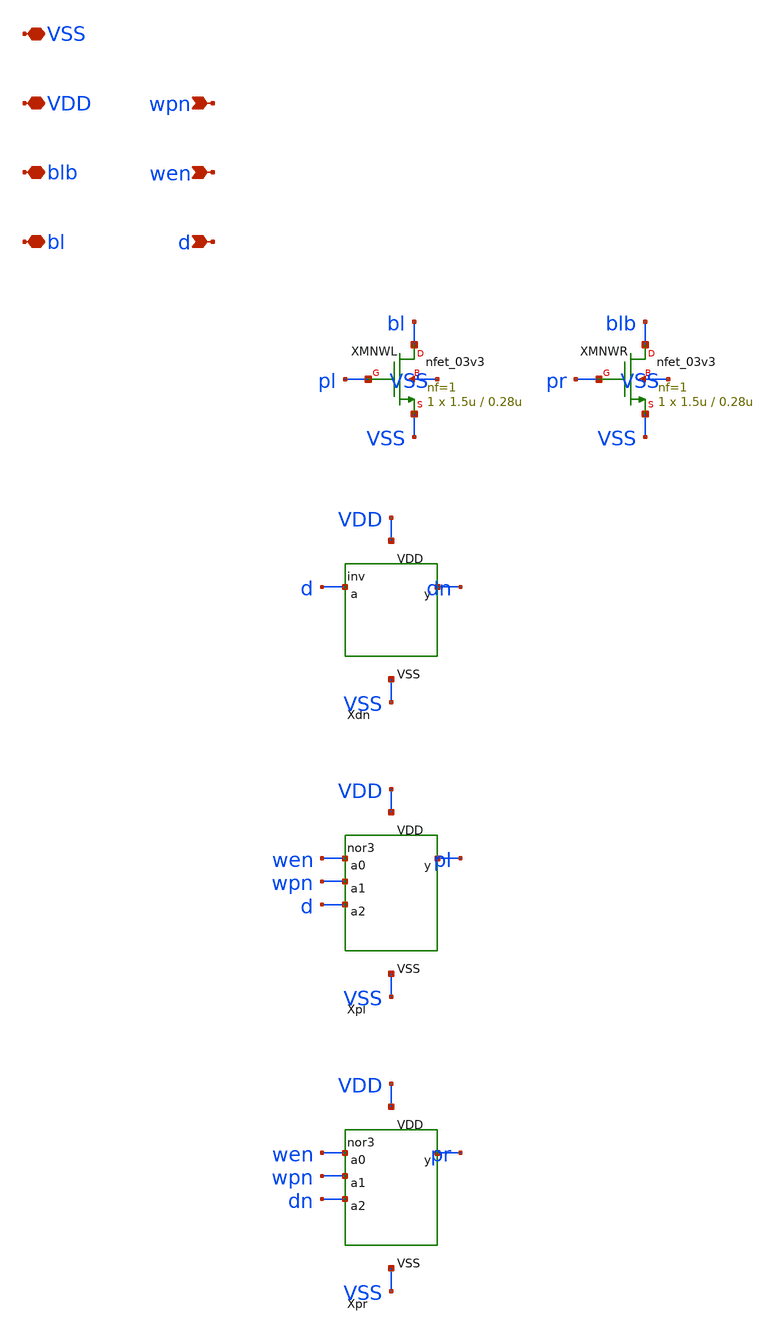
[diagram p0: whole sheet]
** sch_path: design/wdrv.sch
**.subckt wdrv d wen wpn bl blb VDD VSS
*.ipin d
*.ipin wen
*.ipin wpn
*.iopin bl
*.iopin blb
*.iopin VDD
*.iopin VSS
XMNWL bl pl VSS VSS nfet_03v3 L=0.28u W=1.5u nf=1 ad='int((nf+1)/2) * W/nf * 0.18u' as='int((nf+2)/2) * W/nf * 0.18u'
+ pd='2*int((nf+1)/2) * (W/nf + 0.18u)' ps='2*int((nf+2)/2) * (W/nf + 0.18u)' nrd='0.18u / W' nrs='0.18u / W'
+ sa=0 sb=0 sd=0 m=1
XMNWR blb pr VSS VSS nfet_03v3 L=0.28u W=1.5u nf=1 ad='int((nf+1)/2) * W/nf * 0.18u' as='int((nf+2)/2) * W/nf * 0.18u'
+ pd='2*int((nf+1)/2) * (W/nf + 0.18u)' ps='2*int((nf+2)/2) * (W/nf + 0.18u)' nrd='0.18u / W' nrs='0.18u / W'
+ sa=0 sb=0 sd=0 m=1
XXdn d dn VDD VSS inv
XXpl wen wpn d pl VDD VSS nor3
XXpr wen wpn dn pr VDD VSS nor3
**.ends

* expanding   symbol:  inv.sym # of pins=4
** sym_path: design/inv.sym
** sch_path: design/inv.sch
.subckt inv a y VDD VSS

*.ipin a
*.opin y
*.iopin VDD
*.iopin VSS
XMP y a VDD VDD pfet_03v3 L=0.28u W=1u nf=1 ad='int((nf+1)/2) * W/nf * 0.18u' as='int((nf+2)/2) * W/nf * 0.18u'
+ pd='2*int((nf+1)/2) * (W/nf + 0.18u)' ps='2*int((nf+2)/2) * (W/nf + 0.18u)' nrd='0.18u / W' nrs='0.18u / W'
+ sa=0 sb=0 sd=0 m=1
XMN y a VSS VSS nfet_03v3 L=0.28u W=0.5u nf=1 ad='int((nf+1)/2) * W/nf * 0.18u' as='int((nf+2)/2) * W/nf * 0.18u'
+ pd='2*int((nf+1)/2) * (W/nf + 0.18u)' ps='2*int((nf+2)/2) * (W/nf + 0.18u)' nrd='0.18u / W' nrs='0.18u / W'
+ sa=0 sb=0 sd=0 m=1
.ends


* expanding   symbol:  nor3.sym # of pins=6
** sym_path: design/nor3.sym
** sch_path: design/nor3.sch
.subckt nor3 a0 a1 a2 y VDD VSS

*.ipin a0
*.ipin a1
*.ipin a2
*.opin y
*.iopin VDD
*.iopin VSS
XMP0 t1 a0 VDD VDD pfet_03v3 L=0.28u W=2u nf=1 ad='int((nf+1)/2) * W/nf * 0.18u' as='int((nf+2)/2) * W/nf * 0.18u'
+ pd='2*int((nf+1)/2) * (W/nf + 0.18u)' ps='2*int((nf+2)/2) * (W/nf + 0.18u)' nrd='0.18u / W' nrs='0.18u / W'
+ sa=0 sb=0 sd=0 m=1
XMP1 t2 a1 t1 VDD pfet_03v3 L=0.28u W=2u nf=1 ad='int((nf+1)/2) * W/nf * 0.18u' as='int((nf+2)/2) * W/nf * 0.18u'
+ pd='2*int((nf+1)/2) * (W/nf + 0.18u)' ps='2*int((nf+2)/2) * (W/nf + 0.18u)' nrd='0.18u / W' nrs='0.18u / W'
+ sa=0 sb=0 sd=0 m=1
XMP2 y a2 t2 VDD pfet_03v3 L=0.28u W=2u nf=1 ad='int((nf+1)/2) * W/nf * 0.18u' as='int((nf+2)/2) * W/nf * 0.18u'
+ pd='2*int((nf+1)/2) * (W/nf + 0.18u)' ps='2*int((nf+2)/2) * (W/nf + 0.18u)' nrd='0.18u / W' nrs='0.18u / W'
+ sa=0 sb=0 sd=0 m=1
XMN0 y a0 VSS VSS nfet_03v3 L=0.28u W=0.5u nf=1 ad='int((nf+1)/2) * W/nf * 0.18u' as='int((nf+2)/2) * W/nf * 0.18u'
+ pd='2*int((nf+1)/2) * (W/nf + 0.18u)' ps='2*int((nf+2)/2) * (W/nf + 0.18u)' nrd='0.18u / W' nrs='0.18u / W'
+ sa=0 sb=0 sd=0 m=1
XMN1 y a1 VSS VSS nfet_03v3 L=0.28u W=0.5u nf=1 ad='int((nf+1)/2) * W/nf * 0.18u' as='int((nf+2)/2) * W/nf * 0.18u'
+ pd='2*int((nf+1)/2) * (W/nf + 0.18u)' ps='2*int((nf+2)/2) * (W/nf + 0.18u)' nrd='0.18u / W' nrs='0.18u / W'
+ sa=0 sb=0 sd=0 m=1
XMN2 y a2 VSS VSS nfet_03v3 L=0.28u W=0.5u nf=1 ad='int((nf+1)/2) * W/nf * 0.18u' as='int((nf+2)/2) * W/nf * 0.18u'
+ pd='2*int((nf+1)/2) * (W/nf + 0.18u)' ps='2*int((nf+2)/2) * (W/nf + 0.18u)' nrd='0.18u / W' nrs='0.18u / W'
+ sa=0 sb=0 sd=0 m=1
.ends

.end
